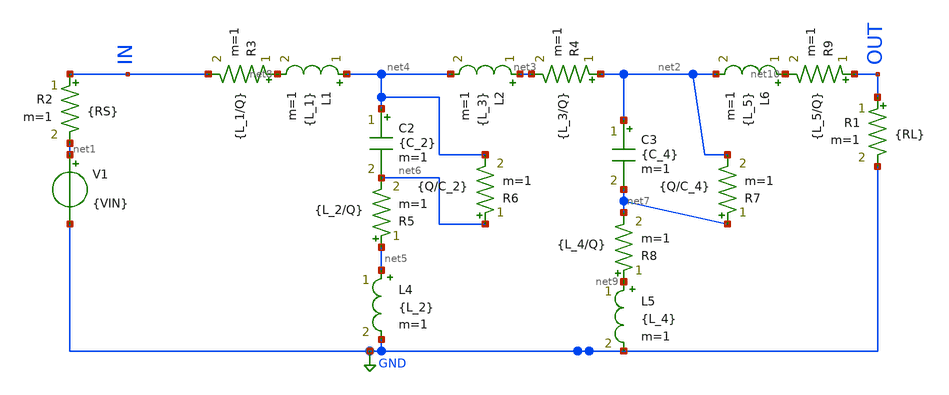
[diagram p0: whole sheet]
** sch_path: LPF design/SCLICAP_TEST/LC_ladder_series_first.sch
**.subckt LC_ladder_series_first
L1 net4 net8 {L_1} m=1
L2 net3 net4 {L_3} m=1
C2 net4 net6 {C_2} m=1
R1 OUT GND {RL} m=1
R2 IN net1 {RS} m=1
V1 net1 GND {VIN}
C3 net2 net7 {C_4} m=1
L4 net5 GND {L_2} m=1
L5 net9 GND {L_4} m=1
L6 net10 net2 {L_5} m=1
R3 net8 IN {L_1/Q} m=1
R4 net2 net3 {L_3/Q} m=1
R5 net5 net6 {L_2/Q} m=1
R6 net6 net4 {Q/C_2} m=1
R7 net7 net2 {Q/C_4} m=1
R8 net9 net7 {L_4/Q} m=1
R9 OUT net10 {L_5/Q} m=1
**.ends
.GLOBAL GND
.end
